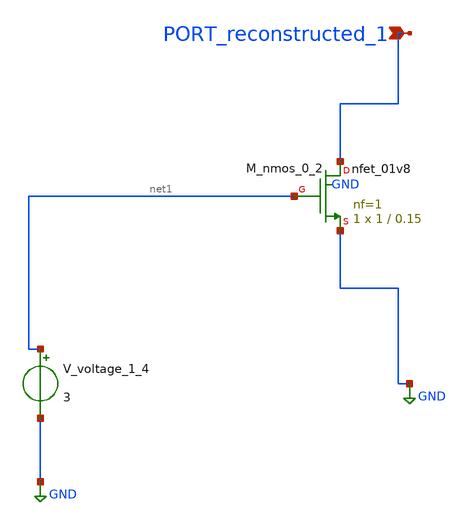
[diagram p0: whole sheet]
** sch_path: schematics/AMSNet/16.sch
**.subckt 16 PORT_reconstructed_1
*.ipin PORT_reconstructed_1
XM_nmos_0_2 PORT_reconstructed_1 net1 GND GND sky130_fd_pr__nfet_01v8 L=0.15 W=1 nf=1 ad='int((1 + 1)/2) * 1 / 1 * 0.29'
+ as='int((1 + 2)/2) * 1 / 1 * 0.29' pd='2*int((1 + 1)/2) * (1 / 1 + 0.29)' ps='2*int((1 + 2)/2) * (1 / 1 + 0.29)'
+ nrd='0.29 / 1 ' nrs='0.29 / 1 ' sa=0 sb=0 sd=0 mult=1 m=1
V_voltage_1_4 net1 GND 3
**.ends
.GLOBAL GND
.end
